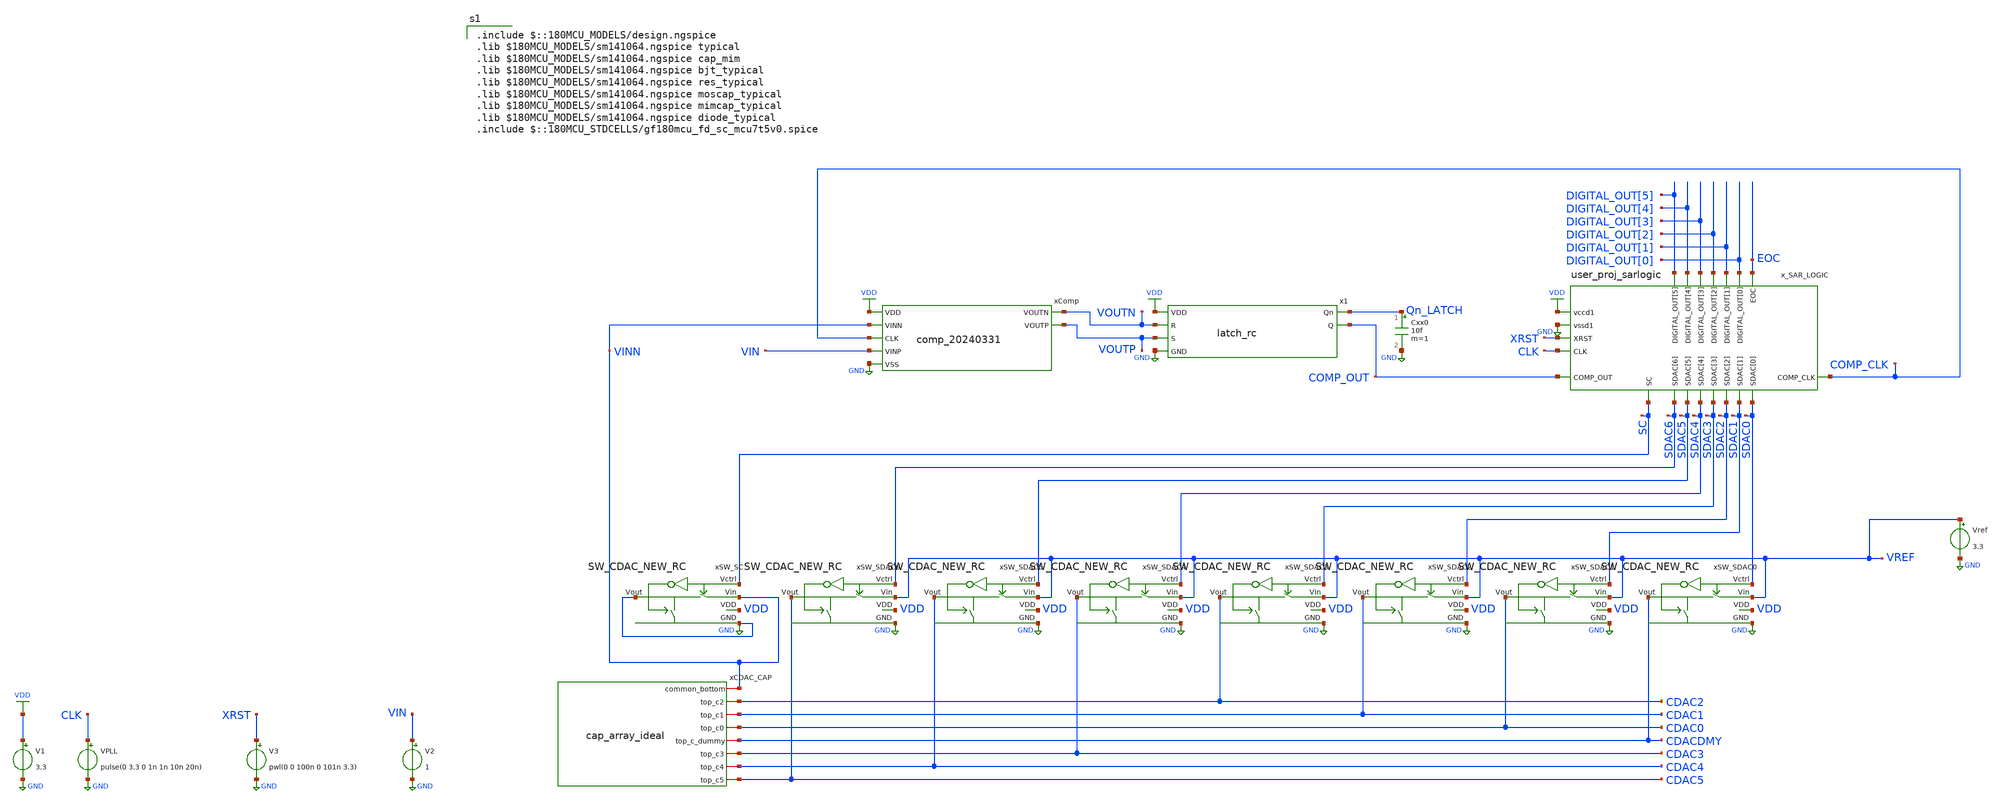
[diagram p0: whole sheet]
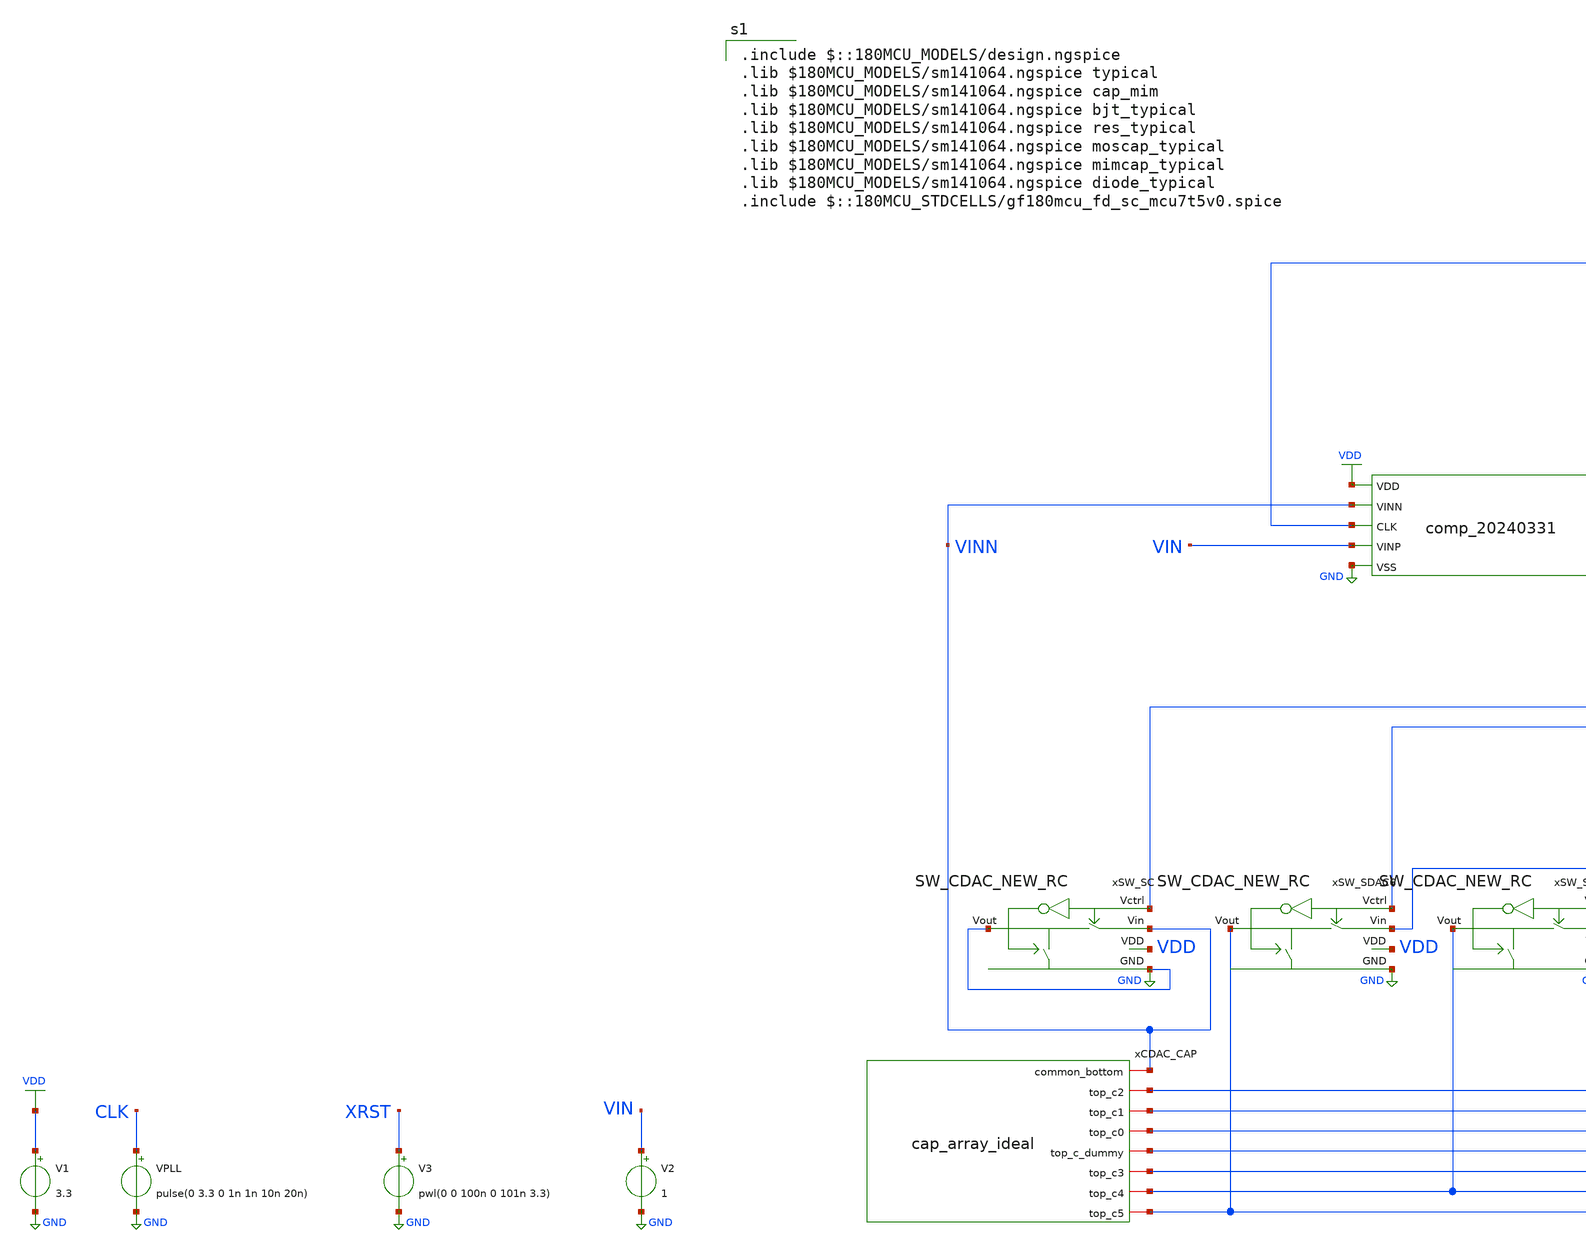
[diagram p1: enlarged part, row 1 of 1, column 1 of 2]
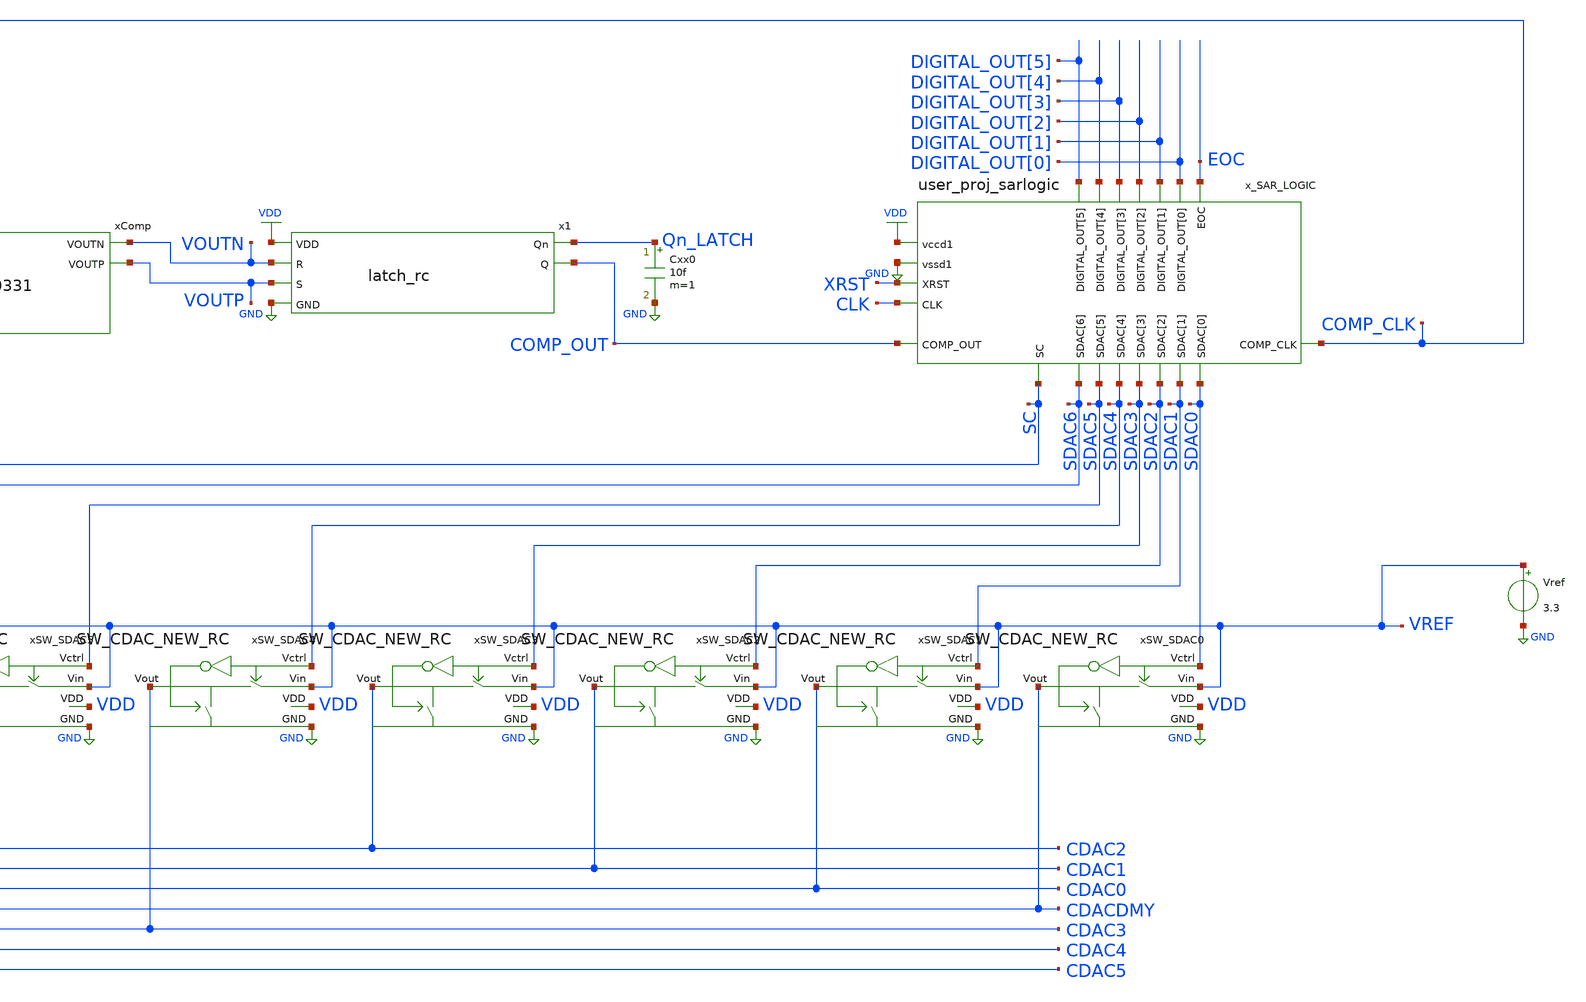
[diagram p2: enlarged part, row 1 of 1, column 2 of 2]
** sch_path: maple0705/SAR_ADC/xschem/tran_sar_adc_CArrayideal.sch
**.subckt tran_sar_adc_CArrayideal
V1 VDD GND 3.3
VPLL CLK GND pulse(0 3.3 0 1n 1n 10n 20n)
x_SAR_LOGIC CLK COMP_CLK COMP_OUT DIGITAL_OUT[0] DIGITAL_OUT[1] DIGITAL_OUT[2] DIGITAL_OUT[3]
+ DIGITAL_OUT[4] DIGITAL_OUT[5] EOC XRST SC SDAC0 SDAC1 SDAC2 SDAC3 SDAC4 SDAC5 SDAC6 VDD GND user_proj_sarlogic
V3 XRST GND pwl(0 0 100n 0 101n 3.3)
xComp VDD COMP_CLK VOUTP VOUTN VIN VINN GND COMP
xSW_SDAC0 VDD SDAC0 GND VREF CDACDMY SW_CDAC
xSW_SDAC1 VDD SDAC1 GND VREF CDAC0 SW_CDAC
xSW_SDAC2 VDD SDAC2 GND VREF CDAC1 SW_CDAC
xSW_SDAC3 VDD SDAC3 GND VREF CDAC2 SW_CDAC
xSW_SDAC4 VDD SDAC4 GND VREF CDAC3 SW_CDAC
xSW_SDAC5 VDD SDAC5 GND VREF CDAC4 SW_CDAC
xSW_SDAC6 VDD SDAC6 GND VREF CDAC5 SW_CDAC
xSW_SC VDD SC GND VINN GND SW_CDAC
Cxx0 Qn_LATCH GND 10f m=1
V2 VIN GND 1
x1 VOUTP VOUTN VDD GND Qn_LATCH COMP_OUT LATCH
Vref VREF GND 3.3
xCDAC_CAP VINN CDAC5 CDAC0 CDAC2 CDAC4 CDAC3 CDACDMY CDAC1 cap_array_ideal
**** begin user architecture code


.include ~/design/Git/Chipathon2023/maple0705/SAR_Logic/klayout/user_proj_sarlogic_pex_extracted.spice
.include ~/design/Git/Chipathon2023/maple0705/SW_CDAC/TOP_pex_extracted.spice
*.include ~/design/Git/Chipathon2023/cdac/mim_cap_array_8x8/rev001/TOP_pex_extracted.spice
.include ~/design/Git/Chipathon2023/latch/TOP_pex_extracted.spice
.include ~/design/Git/Chipathon2023/gitefu/comp_20240331/TOP_pex_extracted.spice
.temp 27
.control
save all
alter V1 3.3

let start_vin = 0.0515625 / 2
let stop_vin = 3.3
let delta_vin = 0.0515625
let vin_act = start_vin
alter V2 vin_act

while vin_act le stop_vin
	tran 100n 1u
	write sar_adc_tran.raw
	meas tran vin FIND v(VIN) WHEN v(EOC)=1.65 FALL=LAST
	meas tran vout5 FIND v(DIGITAL_OUT[5]) WHEN v(EOC)=1.65 FALL=LAST
	meas tran vout4 FIND v(DIGITAL_OUT[4]) WHEN v(EOC)=1.65 FALL=LAST
	meas tran vout3 FIND v(DIGITAL_OUT[3]) WHEN v(EOC)=1.65 FALL=LAST
	meas tran vout2 FIND v(DIGITAL_OUT[2]) WHEN v(EOC)=1.65 FALL=LAST
	meas tran vout1 FIND v(DIGITAL_OUT[1]) WHEN v(EOC)=1.65 FALL=LAST
	meas tran vout0 FIND v(DIGITAL_OUT[0]) WHEN v(EOC)=1.65 FALL=LAST
	print vin >> sar_adc_tran_out_typ_CArrayideal.txt
	print vout5 >> sar_adc_tran_out_typ_CArrayideal.txt
	print vout4 >> sar_adc_tran_out_typ_CArrayideal.txt
	print vout3 >> sar_adc_tran_out_typ_CArrayideal.txt
	print vout2 >> sar_adc_tran_out_typ_CArrayideal.txt
	print vout1 >> sar_adc_tran_out_typ_CArrayideal.txt
	print vout0 >> sar_adc_tran_out_typ_CArrayideal.txt
	let vin_act = vin_act + delta_vin
	alter V2 vin_act
end

.endc



 .include $::180MCU_MODELS/design.ngspice
.lib $180MCU_MODELS/sm141064.ngspice typical
.lib $180MCU_MODELS/sm141064.ngspice cap_mim
.lib $180MCU_MODELS/sm141064.ngspice bjt_typical
.lib $180MCU_MODELS/sm141064.ngspice res_typical
.lib $180MCU_MODELS/sm141064.ngspice moscap_typical
.lib $180MCU_MODELS/sm141064.ngspice mimcap_typical
.lib $180MCU_MODELS/sm141064.ngspice diode_typical
.include $::180MCU_STDCELLS/gf180mcu_fd_sc_mcu7t5v0.spice
**** end user architecture code
**.ends
.GLOBAL GND
.GLOBAL VDD
.end
